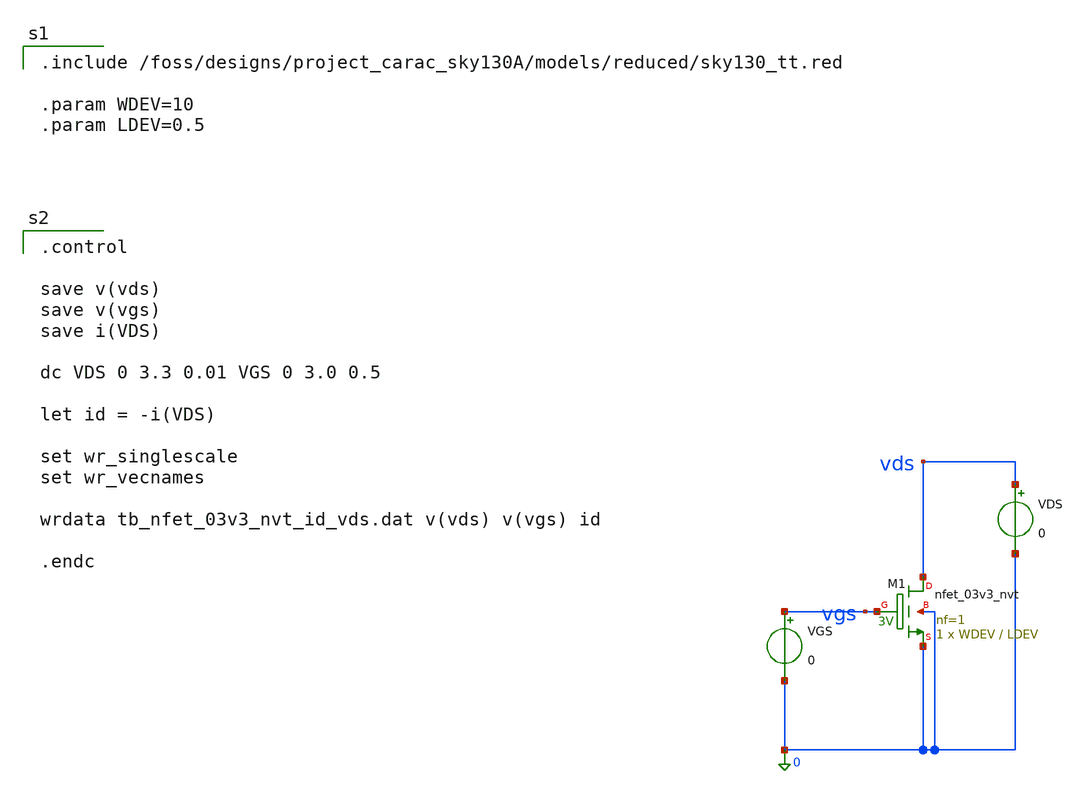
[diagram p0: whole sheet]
** sch_path: dfii/project_carac_sky130A_sim/tb_nfet_03v3_nvt_id_vds.sch
* Copyright 2021 Stefan Frederik Schippers
* Licensed under the Apache License, Version 2.0 (the "License");
* you may not use this file except in compliance with the License.
* You may obtain a copy of the License at
* https://www.apache.org/licenses/LICENSE-2.0
* Unless required by applicable law or agreed to in writing, software
* distributed under the License is distributed on an "AS IS" BASIS,
* WITHOUT WARRANTIES OR CONDITIONS OF ANY KIND, either express or implied.
* See the License for the specific language governing permissions and
* limitations under the License.

.include /foss/designs/project_carac_sky130A/models/reduced/sky130_tt.red

.param WDEV=10
.param LDEV=0.5


**.subckt tb_nfet_03v3_nvt_id_vds
XM1 vds vgs 0 0 sky130_fd_pr__nfet_03v3_nvt L=LDEV W=WDEV nf=1 ad='int((1 + 1)/2) * WDEV / 1 * 0.29'
+ as='int((1 + 2)/2) * WDEV / 1 * 0.29' pd='2*int((1 + 1)/2) * (WDEV / 1 + 0.29)' ps='2*int((1 + 2)/2) * (WDEV / 1 + 0.29)'
+ nrd='0.29 / WDEV ' nrs='0.29 / WDEV ' sa=0 sb=0 sd=0 mult=1 m=1
VGS vgs 0 0
VDS vds 0 0
**.ends
**** begin user architecture code

.control

save v(vds)
save v(vgs)
save i(VDS)

dc VDS 0 3.3 0.01 VGS 0 3.0 0.5

let id = -i(VDS)

set wr_singlescale
set wr_vecnames

wrdata tb_nfet_03v3_nvt_id_vds.dat v(vds) v(vgs) id

.endc

**** end user architecture code
.end
